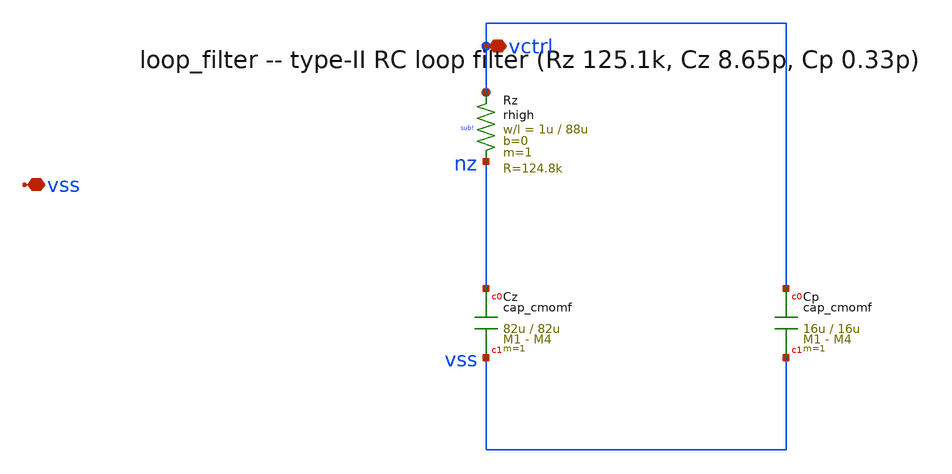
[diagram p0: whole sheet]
** sch_path: xschem/loop_filter_wired.sch
**.subckt loop_filter_wired vctrl vss
*.iopin vctrl
*.iopin vss
XRz vctrl nz sub! rhigh w=1u l=88u m=1 b=0 mm_ok=1
XCz nz vss cap_cmomf w=82u l=82u mmin=1 mmax=4 subblock=0 rfmodel=0 subscale=1 m=1 mm_ok=1
XCp vctrl vss cap_cmomf w=16u l=16u mmin=1 mmax=4 subblock=0 rfmodel=0 subscale=1 m=1 mm_ok=1
**.ends
.end
